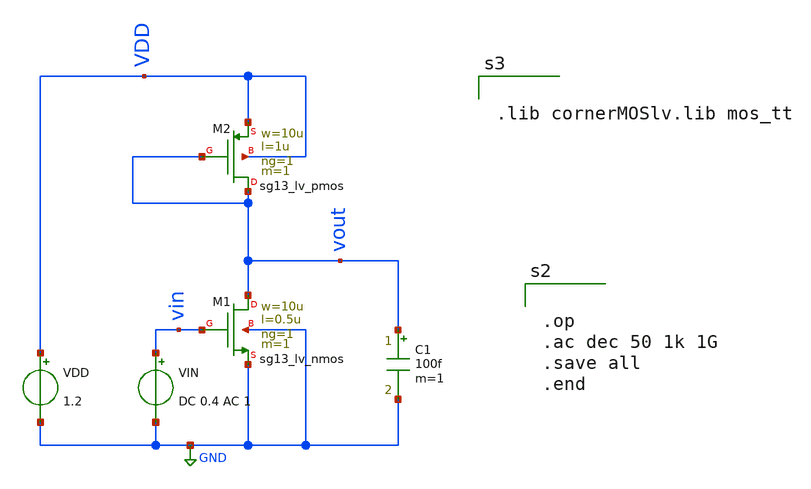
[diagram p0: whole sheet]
** sch_path: BTDay3-Ex/Ex2_Lecture3_1.sch
**.subckt Ex2_Lecture3_1
XM1 vout vin GND GND sg13_lv_nmos w=10u l=0.5u ng=1 m=1 mm_ok=1
VDD VDD GND 1.2
VIN vin GND DC 0.4 AC 1
C1 vout GND 100f m=1
XM2 vout vout VDD VDD sg13_lv_pmos w=10u l=1u ng=1 m=1 mm_ok=1
**** begin user architecture code


.op
.ac dec 50 1k 1G
.save all
.end




.lib cornerMOSlv.lib mos_tt


**** end user architecture code
**.ends
.GLOBAL GND
.end
